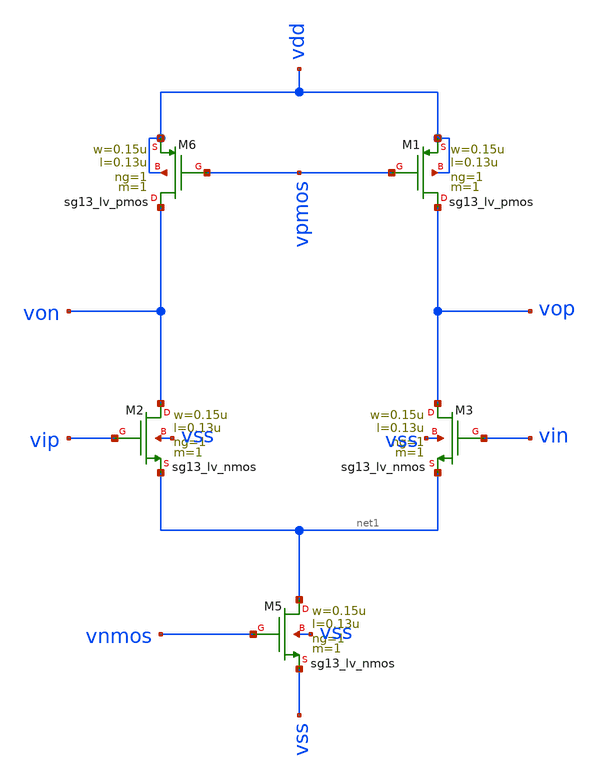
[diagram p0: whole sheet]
** sch_path: xschem/untitled.sch
**.subckt untitled
XM5 net1 vnmos vss vss sg13_lv_nmos w=0.15u l=0.13u ng=1 m=1 mm_ok=1
XM6 von vpmos vdd vdd sg13_lv_pmos w=0.15u l=0.13u ng=1 m=1 mm_ok=1
XM1 vop vpmos vdd vdd sg13_lv_pmos w=0.15u l=0.13u ng=1 m=1 mm_ok=1
XM2 von vip net1 vss sg13_lv_nmos w=0.15u l=0.13u ng=1 m=1 mm_ok=1
XM3 vop vin net1 vss sg13_lv_nmos w=0.15u l=0.13u ng=1 m=1 mm_ok=1
**.ends
.end
